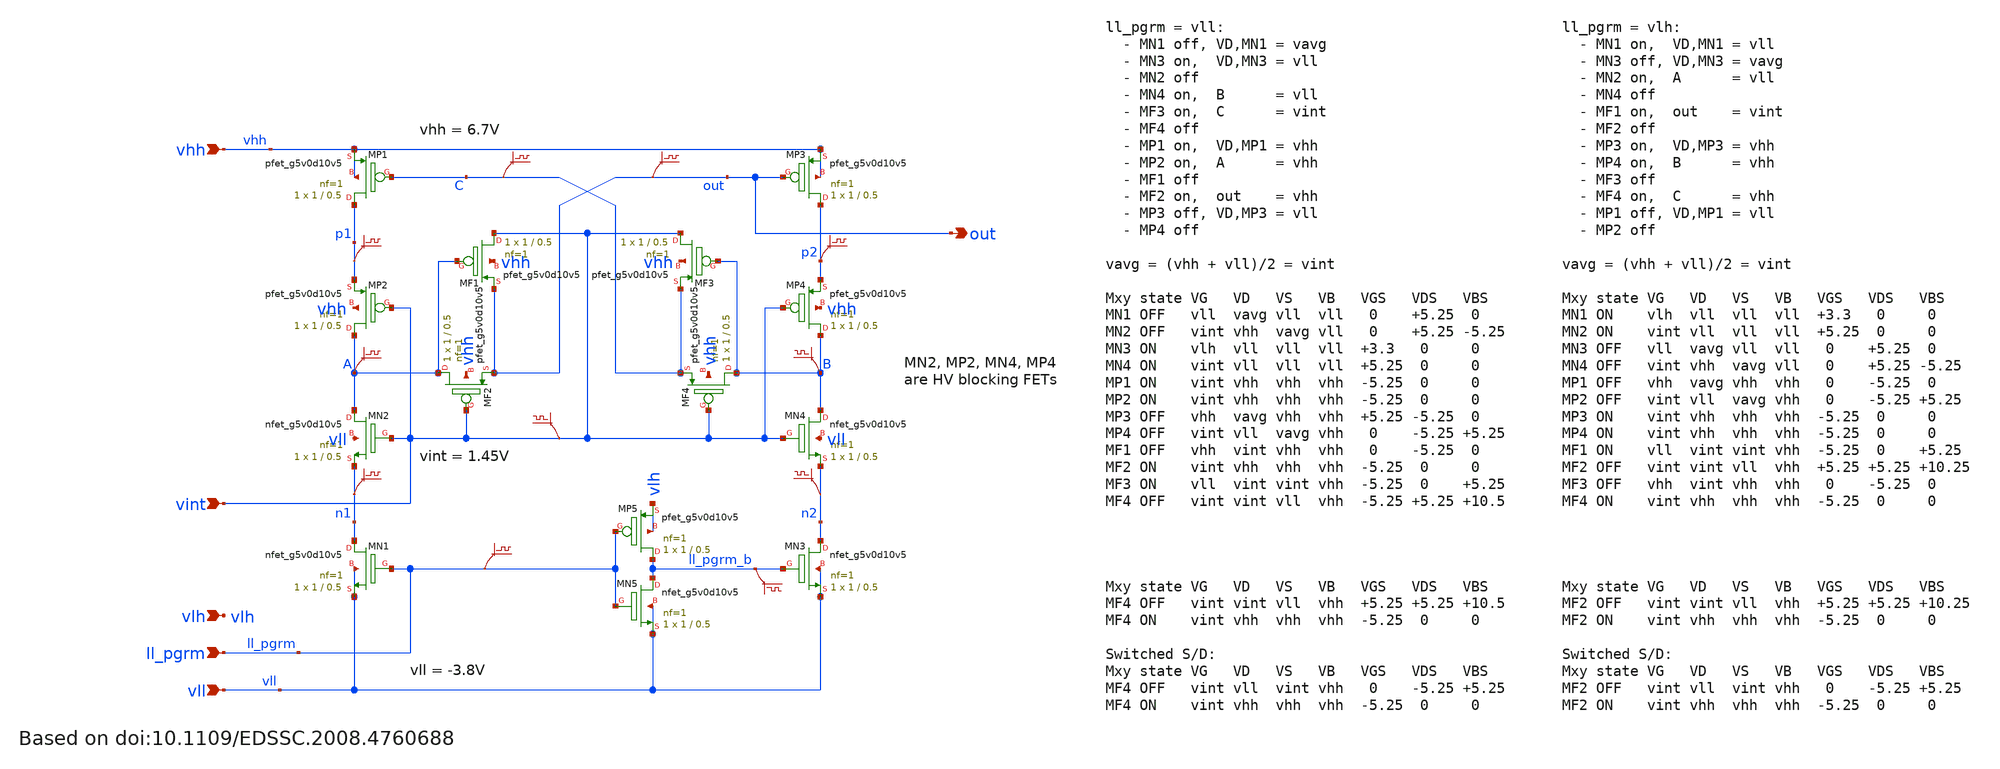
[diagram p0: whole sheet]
** sch_path: hvswitch.sch
**.subckt hvswitch ll_pgrm vhh vll out vlh vint
*.ipin ll_pgrm
*.ipin vhh
*.ipin vll
*.opin out
*.ipin vlh
*.ipin vint
XMN1 n1 ll_pgrm vll vll sky130_fd_pr__nfet_g5v0d10v5 L=0.5 W=1 nf=1 ad='int((nf+1)/2) * W/nf * 0.29'
+ as='int((nf+2)/2) * W/nf * 0.29' pd='2*int((nf+1)/2) * (W/nf + 0.29)' ps='2*int((nf+2)/2) * (W/nf + 0.29)'
+ nrd='0.29 / W' nrs='0.29 / W' sa=0 sb=0 sd=0 mult=1 m=1
XMN2 A vint n1 vll sky130_fd_pr__nfet_g5v0d10v5 L=0.5 W=1 nf=1 ad='int((nf+1)/2) * W/nf * 0.29' as='int((nf+2)/2) * W/nf * 0.29'
+ pd='2*int((nf+1)/2) * (W/nf + 0.29)' ps='2*int((nf+2)/2) * (W/nf + 0.29)' nrd='0.29 / W' nrs='0.29 / W'
+ sa=0 sb=0 sd=0 mult=1 m=1
XMN3 n2 ll_pgrm_b vll vll sky130_fd_pr__nfet_g5v0d10v5 L=0.5 W=1 nf=1 ad='int((nf+1)/2) * W/nf * 0.29'
+ as='int((nf+2)/2) * W/nf * 0.29' pd='2*int((nf+1)/2) * (W/nf + 0.29)' ps='2*int((nf+2)/2) * (W/nf + 0.29)'
+ nrd='0.29 / W' nrs='0.29 / W' sa=0 sb=0 sd=0 mult=1 m=1
XMN4 B vint n2 vll sky130_fd_pr__nfet_g5v0d10v5 L=0.5 W=1 nf=1 ad='int((nf+1)/2) * W/nf * 0.29' as='int((nf+2)/2) * W/nf * 0.29'
+ pd='2*int((nf+1)/2) * (W/nf + 0.29)' ps='2*int((nf+2)/2) * (W/nf + 0.29)' nrd='0.29 / W' nrs='0.29 / W'
+ sa=0 sb=0 sd=0 mult=1 m=1
XMP1 p1 C vhh vhh sky130_fd_pr__pfet_g5v0d10v5 L=0.5 W=1 nf=1 ad='int((nf+1)/2) * W/nf * 0.29' as='int((nf+2)/2) * W/nf * 0.29'
+ pd='2*int((nf+1)/2) * (W/nf + 0.29)' ps='2*int((nf+2)/2) * (W/nf + 0.29)' nrd='0.29 / W' nrs='0.29 / W'
+ sa=0 sb=0 sd=0 mult=1 m=1
XMP2 A vint p1 vhh sky130_fd_pr__pfet_g5v0d10v5 L=0.5 W=1 nf=1 ad='int((nf+1)/2) * W/nf * 0.29' as='int((nf+2)/2) * W/nf * 0.29'
+ pd='2*int((nf+1)/2) * (W/nf + 0.29)' ps='2*int((nf+2)/2) * (W/nf + 0.29)' nrd='0.29 / W' nrs='0.29 / W'
+ sa=0 sb=0 sd=0 mult=1 m=1
XMP3 p2 out vhh vhh sky130_fd_pr__pfet_g5v0d10v5 L=0.5 W=1 nf=1 ad='int((nf+1)/2) * W/nf * 0.29' as='int((nf+2)/2) * W/nf * 0.29'
+ pd='2*int((nf+1)/2) * (W/nf + 0.29)' ps='2*int((nf+2)/2) * (W/nf + 0.29)' nrd='0.29 / W' nrs='0.29 / W'
+ sa=0 sb=0 sd=0 mult=1 m=1
XMP4 B vint p2 vhh sky130_fd_pr__pfet_g5v0d10v5 L=0.5 W=1 nf=1 ad='int((nf+1)/2) * W/nf * 0.29' as='int((nf+2)/2) * W/nf * 0.29'
+ pd='2*int((nf+1)/2) * (W/nf + 0.29)' ps='2*int((nf+2)/2) * (W/nf + 0.29)' nrd='0.29 / W' nrs='0.29 / W'
+ sa=0 sb=0 sd=0 mult=1 m=1
XMF1 vint A out vhh sky130_fd_pr__pfet_g5v0d10v5 L=0.5 W=1 nf=1 ad='int((nf+1)/2) * W/nf * 0.29' as='int((nf+2)/2) * W/nf * 0.29'
+ pd='2*int((nf+1)/2) * (W/nf + 0.29)' ps='2*int((nf+2)/2) * (W/nf + 0.29)' nrd='0.29 / W' nrs='0.29 / W'
+ sa=0 sb=0 sd=0 mult=1 m=1
XMF2 A vint out vhh sky130_fd_pr__pfet_g5v0d10v5 L=0.5 W=1 nf=1 ad='int((nf+1)/2) * W/nf * 0.29' as='int((nf+2)/2) * W/nf * 0.29'
+ pd='2*int((nf+1)/2) * (W/nf + 0.29)' ps='2*int((nf+2)/2) * (W/nf + 0.29)' nrd='0.29 / W' nrs='0.29 / W'
+ sa=0 sb=0 sd=0 mult=1 m=1
XMF3 vint B C vhh sky130_fd_pr__pfet_g5v0d10v5 L=0.5 W=1 nf=1 ad='int((nf+1)/2) * W/nf * 0.29' as='int((nf+2)/2) * W/nf * 0.29'
+ pd='2*int((nf+1)/2) * (W/nf + 0.29)' ps='2*int((nf+2)/2) * (W/nf + 0.29)' nrd='0.29 / W' nrs='0.29 / W'
+ sa=0 sb=0 sd=0 mult=1 m=1
XMF4 B vint C vhh sky130_fd_pr__pfet_g5v0d10v5 L=0.5 W=1 nf=1 ad='int((nf+1)/2) * W/nf * 0.29' as='int((nf+2)/2) * W/nf * 0.29'
+ pd='2*int((nf+1)/2) * (W/nf + 0.29)' ps='2*int((nf+2)/2) * (W/nf + 0.29)' nrd='0.29 / W' nrs='0.29 / W'
+ sa=0 sb=0 sd=0 mult=1 m=1
XMP5 ll_pgrm_b ll_pgrm vlh vlh sky130_fd_pr__pfet_g5v0d10v5 L=0.5 W=1 nf=1 ad='int((nf+1)/2) * W/nf * 0.29'
+ as='int((nf+2)/2) * W/nf * 0.29' pd='2*int((nf+1)/2) * (W/nf + 0.29)' ps='2*int((nf+2)/2) * (W/nf + 0.29)'
+ nrd='0.29 / W' nrs='0.29 / W' sa=0 sb=0 sd=0 mult=1 m=1
XMN5 ll_pgrm_b ll_pgrm vll vll sky130_fd_pr__nfet_g5v0d10v5 L=0.5 W=1 nf=1 ad='int((nf+1)/2) * W/nf * 0.29'
+ as='int((nf+2)/2) * W/nf * 0.29' pd='2*int((nf+1)/2) * (W/nf + 0.29)' ps='2*int((nf+2)/2) * (W/nf + 0.29)'
+ nrd='0.29 / W' nrs='0.29 / W' sa=0 sb=0 sd=0 mult=1 m=1
.save v(a)
.save v(b)
.save v(c)
.save v(out)
.save v(p1)
.save v(p2)
.save v(n1)
.save v(n2)
.save v(vint)
.save v(ll_pgrm)
.save v(ll_pgrm_b)
**.ends
.end
